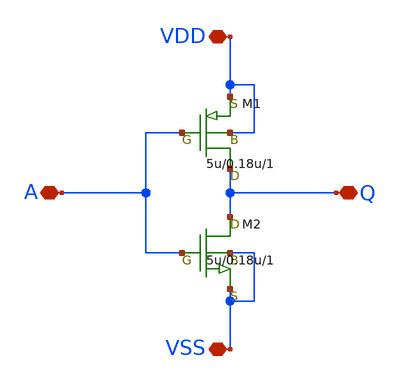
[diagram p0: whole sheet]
** sch_path: inverter.sch
**.subckt inverter VDD A Q VSS
*.iopin VDD
*.iopin A
*.iopin Q
*.iopin VSS
M1 Q A VDD VDD pch w=5u l=0.18u as=0 ps=0 ad=0 pd=0 m=1
M2 Q A VSS VSS nch w=5u l=0.18u as=0 ps=0 ad=0 pd=0 m=1
**.ends
.end
